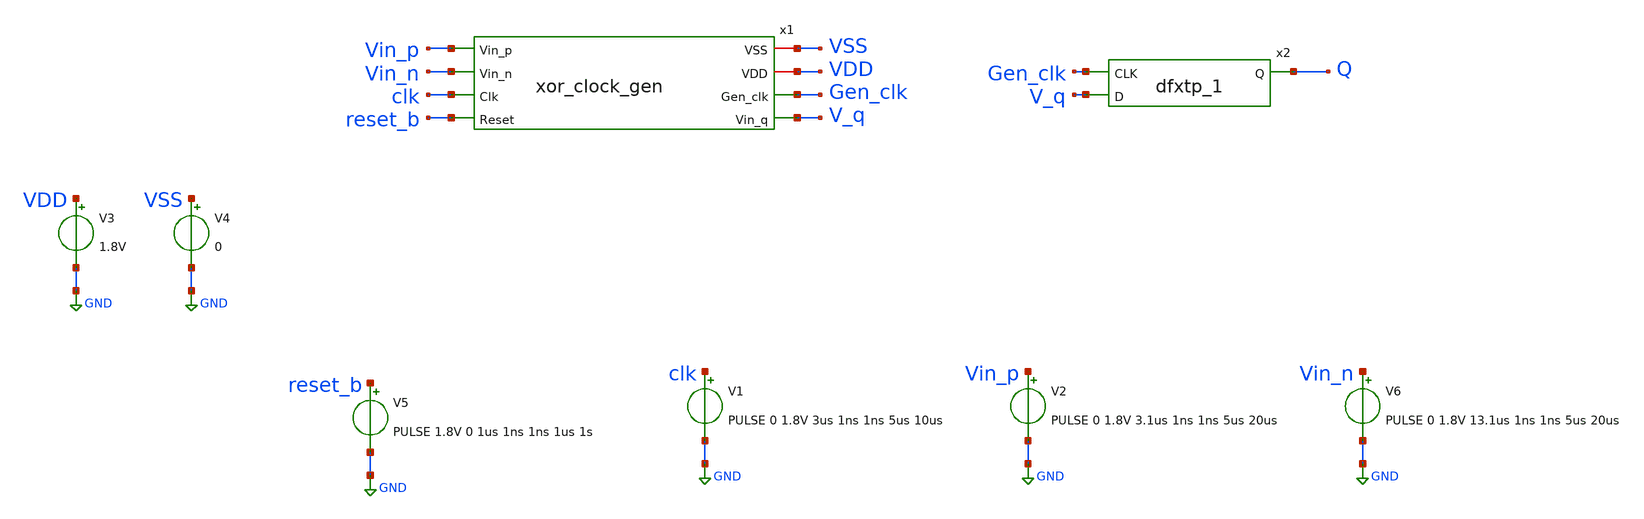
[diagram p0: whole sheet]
** sch_path: xschem/tests/xor_clock_gen/xor_clock_gen_timing_test.sch
**.subckt xor_clock_gen_timing_test
V3 VDD GND 1.8V
V4 VSS GND 0
x1 VSS Vin_p VDD Vin_n Gen_clk clk V_q reset_b xor_clock_gen
V5 reset_b GND PULSE 1.8V 0 1us 1ns 1ns 1us 1s
V1 clk GND PULSE 0 1.8V 3us 1ns 1ns 5us 10us
V2 Vin_p GND PULSE 0 1.8V 3.1us 1ns 1ns 5us 20us
V6 Vin_n GND PULSE 0 1.8V 13.1us 1ns 1ns 5us 20us
x2 Gen_clk V_q VSS VSS VDD VDD Q sky130_fd_sc_hd__dfxtp_1
**** begin user architecture code
 .lib $::SKYWATER_MODELS/sky130.lib.spice tt
.include $::SKYWATER_STDCELLS/sky130_fd_sc_hd.spice


.options acct list
.temp 25
*vvcc VDD 0 dc 1.8
*vvss VSS 0 0
.control
tran 0.01u 11u
*plot RST_PLS clk+2 Pulse+4
plot Vin_p-Vin_n clk reset_b-2 Gen_clk Q+2 Q2+4
write xor_clock_gen_timing_test.raw
.endc


**** end user architecture code
**.ends
.GLOBAL GND
.end
